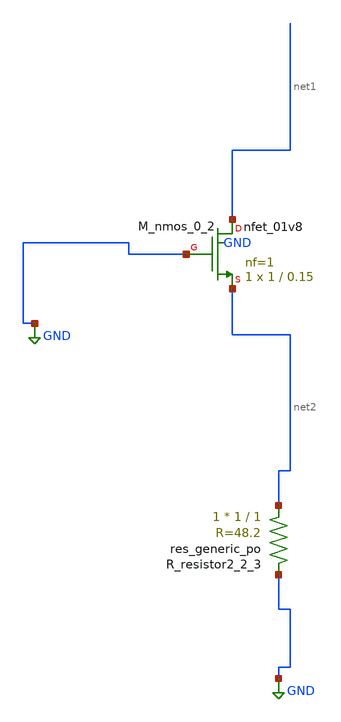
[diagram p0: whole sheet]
** sch_path: schematics/AMSNet/133.sch
**.subckt 133
XM_nmos_0_2 net1 GND net2 GND sky130_fd_pr__nfet_01v8 L=0.15 W=1 nf=1 ad='int((1 + 1)/2) * 1 / 1 * 0.29'
+ as='int((1 + 2)/2) * 1 / 1 * 0.29' pd='2*int((1 + 1)/2) * (1 / 1 + 0.29)' ps='2*int((1 + 2)/2) * (1 / 1 + 0.29)'
+ nrd='0.29 / 1 ' nrs='0.29 / 1 ' sa=0 sb=0 sd=0 mult=1 m=1
XR_resistor2_2_3 net2 GND sky130_fd_pr__res_generic_po W=1 L=1 m=1
**.ends
.GLOBAL GND
.end
